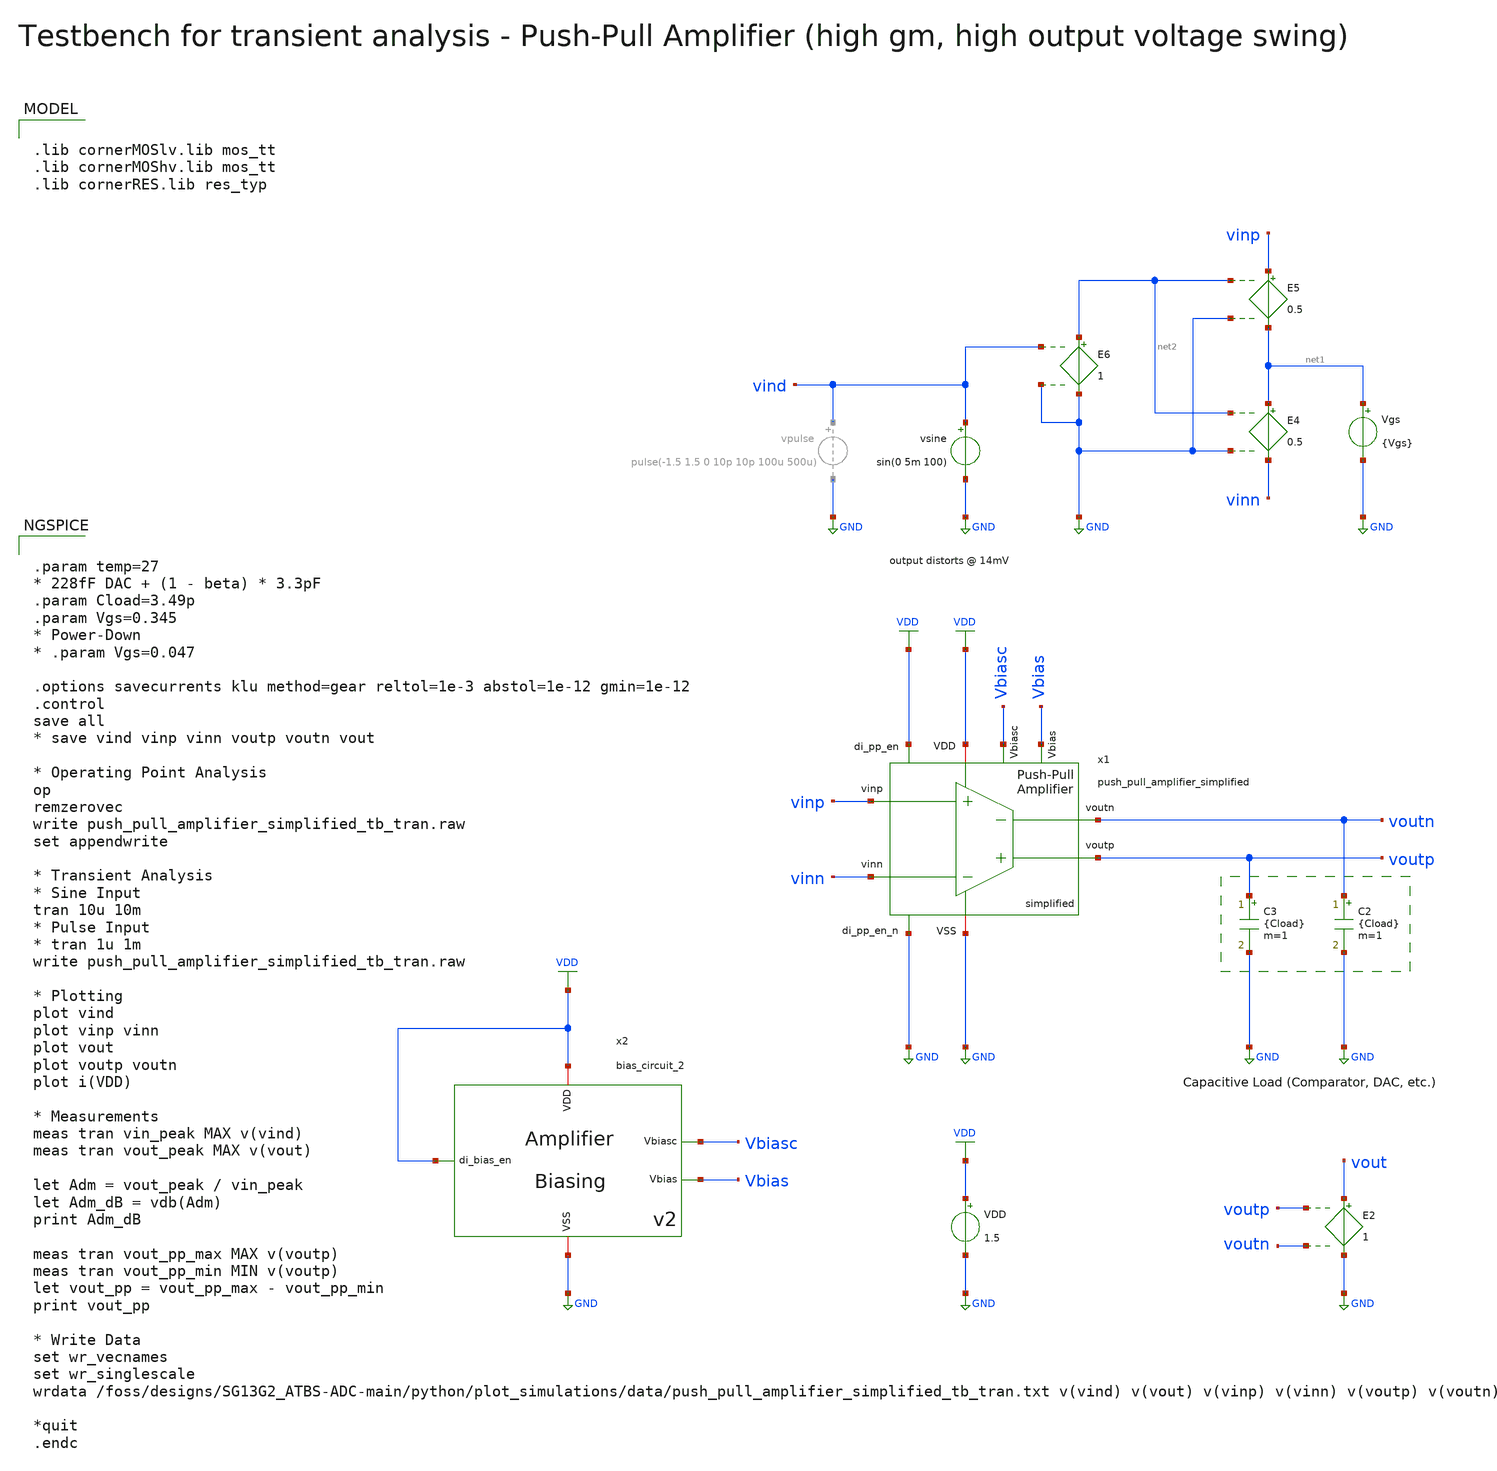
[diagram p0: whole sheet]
** sch_path: SG13G2_ATBS-ADC-main/xschem/bio_amplifier/amplifier_core/push_pull_amplifier/testbenches/push_pull_amplifier_simplified_tb_tran.sch
**.subckt push_pull_amplifier_simplified_tb_tran
VDD VDD GND 1.5
Vgs net1 GND {Vgs}
E4 net1 vinn net2 GND 0.5
E5 vinp net1 net2 GND 0.5
E6 net2 GND vind GND 1
C2 voutn GND {Cload} m=1
C3 voutp GND {Cload} m=1
vsine vind GND sin(0 5m 100)
E2 vout GND voutp voutn 1
x1 VDD voutp voutn vinn vinp GND GND VDD Vbiasc Vbias push_pull_amplifier_simplified
x2 VDD Vbiasc VDD GND Vbias bias_circuit_2
**** begin user architecture code


.param temp=27
* 228fF DAC + (1 - beta) * 3.3pF
.param Cload=3.49p
.param Vgs=0.345
* Power-Down
* .param Vgs=0.047

.options savecurrents klu method=gear reltol=1e-3 abstol=1e-12 gmin=1e-12
.control
save all
* save vind vinp vinn voutp voutn vout

* Operating Point Analysis
op
remzerovec
write push_pull_amplifier_simplified_tb_tran.raw
set appendwrite

* Transient Analysis
* Sine Input
tran 10u 10m
* Pulse Input
* tran 1u 1m
write push_pull_amplifier_simplified_tb_tran.raw

* Plotting
plot vind
plot vinp vinn
plot vout
plot voutp voutn
plot i(VDD)

* Measurements
meas tran vin_peak MAX v(vind)
meas tran vout_peak MAX v(vout)

let Adm = vout_peak / vin_peak
let Adm_dB = vdb(Adm)
print Adm_dB

meas tran vout_pp_max MAX v(voutp)
meas tran vout_pp_min MIN v(voutp)
let vout_pp = vout_pp_max - vout_pp_min
print vout_pp

* Write Data
set wr_vecnames
set wr_singlescale
wrdata
+ /foss/designs/SG13G2_ATBS-ADC-main/python/plot_simulations/data/push_pull_amplifier_simplified_tb_tran.txt v(vind) v(vout) v(vinp) v(vinn) v(voutp) v(voutn)

*quit
.endc



.lib cornerMOSlv.lib mos_tt
.lib cornerMOShv.lib mos_tt
.lib cornerRES.lib res_typ

**** end user architecture code
**.ends
.GLOBAL GND
.GLOBAL VDD
.end
